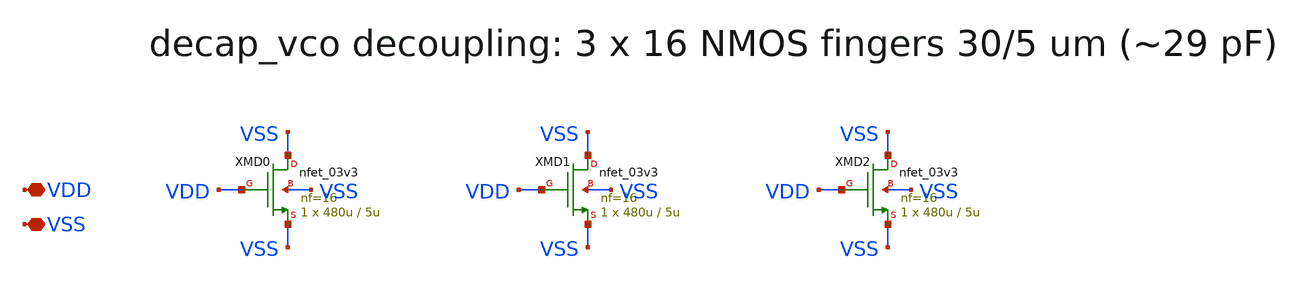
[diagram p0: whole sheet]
** sch_path: xschem/decap_vco.sch
**.subckt decap_vco VDD VSS
*.iopin VDD
*.iopin VSS
XMD0 VSS VDD VSS VSS nfet_03v3 L=5u W=480u nf=16 ad='int((nf+1)/2) * W/nf * 0.18u' as='int((nf+2)/2) * W/nf * 0.18u'
+ pd='2*int((nf+1)/2) * (W/nf + 0.18u)' ps='2*int((nf+2)/2) * (W/nf + 0.18u)' nrd='0.18u / W' nrs='0.18u / W'
+ sa=0 sb=0 sd=0 m=1
XMD1 VSS VDD VSS VSS nfet_03v3 L=5u W=480u nf=16 ad='int((nf+1)/2) * W/nf * 0.18u' as='int((nf+2)/2) * W/nf * 0.18u'
+ pd='2*int((nf+1)/2) * (W/nf + 0.18u)' ps='2*int((nf+2)/2) * (W/nf + 0.18u)' nrd='0.18u / W' nrs='0.18u / W'
+ sa=0 sb=0 sd=0 m=1
XMD2 VSS VDD VSS VSS nfet_03v3 L=5u W=480u nf=16 ad='int((nf+1)/2) * W/nf * 0.18u' as='int((nf+2)/2) * W/nf * 0.18u'
+ pd='2*int((nf+1)/2) * (W/nf + 0.18u)' ps='2*int((nf+2)/2) * (W/nf + 0.18u)' nrd='0.18u / W' nrs='0.18u / W'
+ sa=0 sb=0 sd=0 m=1
**.ends
.end
